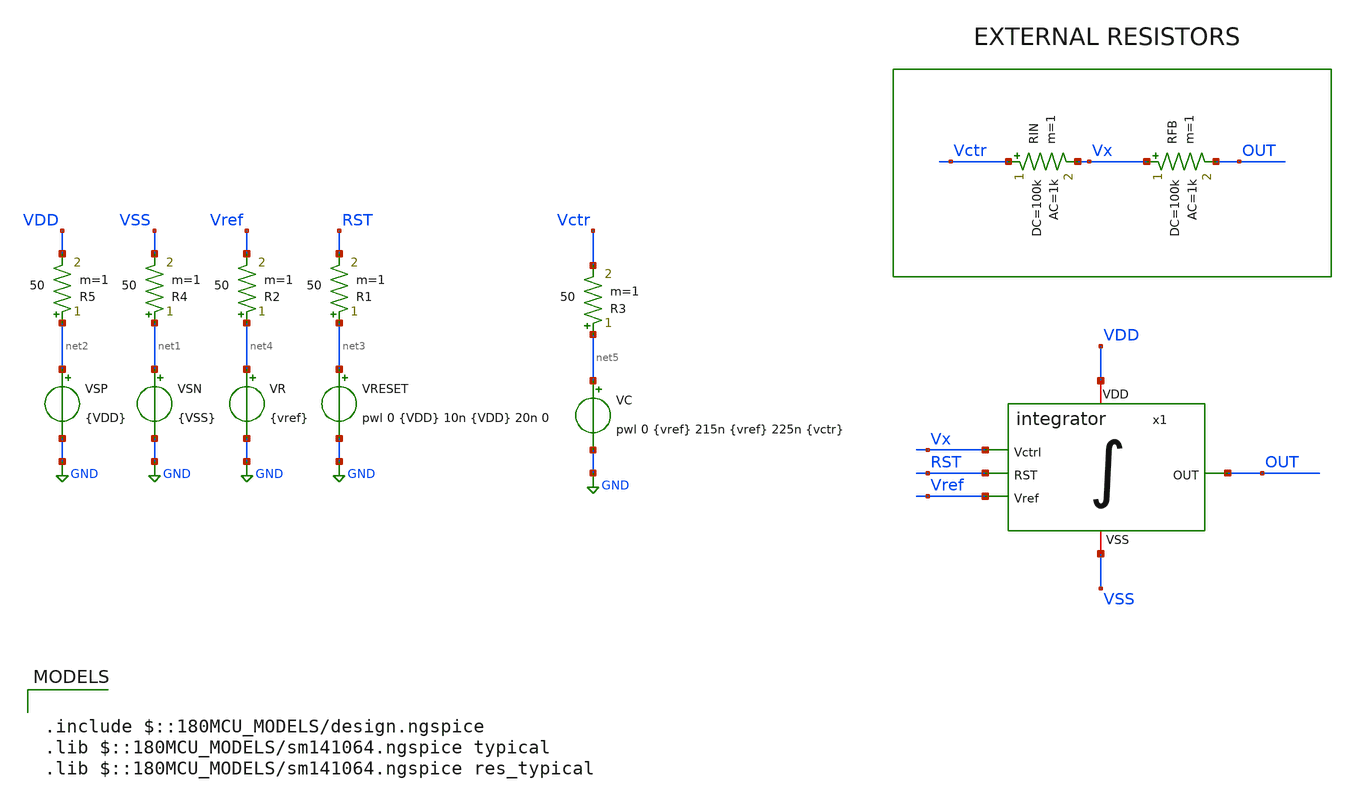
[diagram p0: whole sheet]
** sch_path: designs/integrator/xschem/integrator_LPF_TB.sch
**.subckt integrator_LPF_TB
VRESET net3 GND pwl 0 {VDD} 10n {VDD} 20n 0
VSP net2 GND {VDD}
VSN net1 GND {VSS}
VR net4 GND {vref}
VC net5 GND pwl 0 {vref} 215n {vref} 225n {vctr}
RIN Vctr Vx 100k ac=1k m=1
RFB Vx OUT 100k ac=1k m=1
R3 net5 Vctr 50 m=1
R1 net3 RST 50 m=1
R2 net4 Vref 50 m=1
R4 net1 VSS 50 m=1
R5 net2 VDD 50 m=1
x1 VDD Vx OUT RST Vref VSS integrator
**** begin user architecture code

.include $::180MCU_MODELS/design.ngspice
.lib $::180MCU_MODELS/sm141064.ngspice typical
.lib $::180MCU_MODELS/sm141064.ngspice res_typical





.param VDD = 1.8
.param VSS = 0
.param vctr = 1
.param vref = 1.3
.param cap = 15f

.param wxor=5.6u

.save all

.control

*----------------------------- Parámetros generales
let Vhigh = 1.8
let Vmid = Vhigh * 0.5

tran 0.1n 1u
meas tran IDD_AVG AVG i(VSP) from=20n to=1u
let PAVG = abs(IDD_AVG*Vhigh)
print PAVG

meas TRAN T_period TRIG v(B) VAL=Vmid rise=2 TARG v(B) VAL=Vmid rise=3
let F_ring = 1 / T_period
print F_ring

plot v(Vctr) v(Vref)
plot v(OUT) v(Vx)
plot v(RST)

.endc


**** end user architecture code
**.ends
.GLOBAL GND
.end
